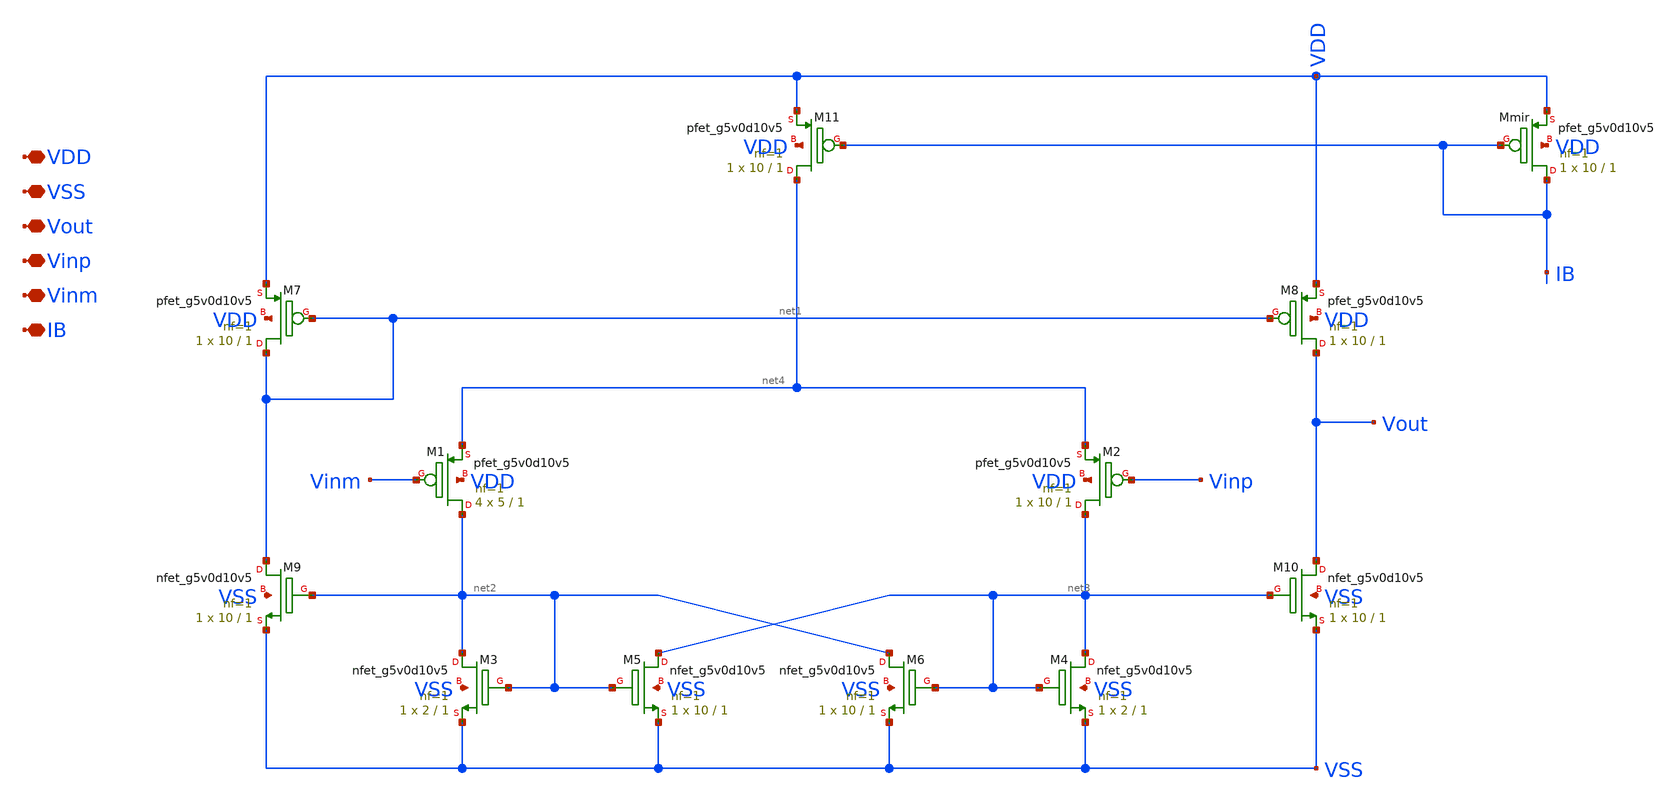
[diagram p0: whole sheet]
** sch_path: design/comparator/comparator.sch
**.subckt comparator VDD VSS Vout Vinp Vinm IB
*.iopin VDD
*.iopin VSS
*.iopin Vout
*.iopin Vinp
*.iopin Vinm
*.iopin IB
XM3 net2 net2 VSS VSS sky130_fd_pr__nfet_g5v0d10v5 L=1 W=2 nf=1 ad='int((nf+1)/2) * W/nf * 0.29' as='int((nf+2)/2) * W/nf * 0.29'
+ pd='2*int((nf+1)/2) * (W/nf + 0.29)' ps='2*int((nf+2)/2) * (W/nf + 0.29)' nrd='0.29 / W' nrs='0.29 / W'
+ sa=0 sb=0 sd=0 mult=1 m=1
XM5 net3 net2 VSS VSS sky130_fd_pr__nfet_g5v0d10v5 L=1 W=10 nf=1 ad='int((nf+1)/2) * W/nf * 0.29' as='int((nf+2)/2) * W/nf * 0.29'
+ pd='2*int((nf+1)/2) * (W/nf + 0.29)' ps='2*int((nf+2)/2) * (W/nf + 0.29)' nrd='0.29 / W' nrs='0.29 / W'
+ sa=0 sb=0 sd=0 mult=1 m=1
XM4 net3 net3 VSS VSS sky130_fd_pr__nfet_g5v0d10v5 L=1 W=2 nf=1 ad='int((nf+1)/2) * W/nf * 0.29' as='int((nf+2)/2) * W/nf * 0.29'
+ pd='2*int((nf+1)/2) * (W/nf + 0.29)' ps='2*int((nf+2)/2) * (W/nf + 0.29)' nrd='0.29 / W' nrs='0.29 / W'
+ sa=0 sb=0 sd=0 mult=1 m=1
XM11 net4 IB VDD VDD sky130_fd_pr__pfet_g5v0d10v5 L=1 W=10 nf=1 ad='int((nf+1)/2) * W/nf * 0.29' as='int((nf+2)/2) * W/nf * 0.29'
+ pd='2*int((nf+1)/2) * (W/nf + 0.29)' ps='2*int((nf+2)/2) * (W/nf + 0.29)' nrd='0.29 / W' nrs='0.29 / W'
+ sa=0 sb=0 sd=0 mult=1 m=1
XM8 Vout net1 VDD VDD sky130_fd_pr__pfet_g5v0d10v5 L=1 W=10 nf=1 ad='int((nf+1)/2) * W/nf * 0.29' as='int((nf+2)/2) * W/nf * 0.29'
+ pd='2*int((nf+1)/2) * (W/nf + 0.29)' ps='2*int((nf+2)/2) * (W/nf + 0.29)' nrd='0.29 / W' nrs='0.29 / W'
+ sa=0 sb=0 sd=0 mult=1 m=1
XM7 net1 net1 VDD VDD sky130_fd_pr__pfet_g5v0d10v5 L=1 W=10 nf=1 ad='int((nf+1)/2) * W/nf * 0.29' as='int((nf+2)/2) * W/nf * 0.29'
+ pd='2*int((nf+1)/2) * (W/nf + 0.29)' ps='2*int((nf+2)/2) * (W/nf + 0.29)' nrd='0.29 / W' nrs='0.29 / W'
+ sa=0 sb=0 sd=0 mult=1 m=1
XM2 net3 Vinp net4 VDD sky130_fd_pr__pfet_g5v0d10v5 L=1 W=10 nf=1 ad='int((nf+1)/2) * W/nf * 0.29' as='int((nf+2)/2) * W/nf * 0.29'
+ pd='2*int((nf+1)/2) * (W/nf + 0.29)' ps='2*int((nf+2)/2) * (W/nf + 0.29)' nrd='0.29 / W' nrs='0.29 / W'
+ sa=0 sb=0 sd=0 mult=1 m=1
XM1 net2 Vinm net4 VDD sky130_fd_pr__pfet_g5v0d10v5 L=1 W=5 nf=1 ad='int((nf+1)/2) * W/nf * 0.29' as='int((nf+2)/2) * W/nf * 0.29'
+ pd='2*int((nf+1)/2) * (W/nf + 0.29)' ps='2*int((nf+2)/2) * (W/nf + 0.29)' nrd='0.29 / W' nrs='0.29 / W'
+ sa=0 sb=0 sd=0 mult=4 m=4
XMmir IB IB VDD VDD sky130_fd_pr__pfet_g5v0d10v5 L=1 W=10 nf=1 ad='int((nf+1)/2) * W/nf * 0.29' as='int((nf+2)/2) * W/nf * 0.29'
+ pd='2*int((nf+1)/2) * (W/nf + 0.29)' ps='2*int((nf+2)/2) * (W/nf + 0.29)' nrd='0.29 / W' nrs='0.29 / W'
+ sa=0 sb=0 sd=0 mult=1 m=1
XM6 net2 net3 VSS VSS sky130_fd_pr__nfet_g5v0d10v5 L=1 W=10 nf=1 ad='int((nf+1)/2) * W/nf * 0.29' as='int((nf+2)/2) * W/nf * 0.29'
+ pd='2*int((nf+1)/2) * (W/nf + 0.29)' ps='2*int((nf+2)/2) * (W/nf + 0.29)' nrd='0.29 / W' nrs='0.29 / W'
+ sa=0 sb=0 sd=0 mult=1 m=1
XM9 net1 net2 VSS VSS sky130_fd_pr__nfet_g5v0d10v5 L=1 W=10 nf=1 ad='int((nf+1)/2) * W/nf * 0.29' as='int((nf+2)/2) * W/nf * 0.29'
+ pd='2*int((nf+1)/2) * (W/nf + 0.29)' ps='2*int((nf+2)/2) * (W/nf + 0.29)' nrd='0.29 / W' nrs='0.29 / W'
+ sa=0 sb=0 sd=0 mult=1 m=1
XM10 Vout net3 VSS VSS sky130_fd_pr__nfet_g5v0d10v5 L=1 W=10 nf=1 ad='int((nf+1)/2) * W/nf * 0.29' as='int((nf+2)/2) * W/nf * 0.29'
+ pd='2*int((nf+1)/2) * (W/nf + 0.29)' ps='2*int((nf+2)/2) * (W/nf + 0.29)' nrd='0.29 / W' nrs='0.29 / W'
+ sa=0 sb=0 sd=0 mult=1 m=1
**.ends
.end
